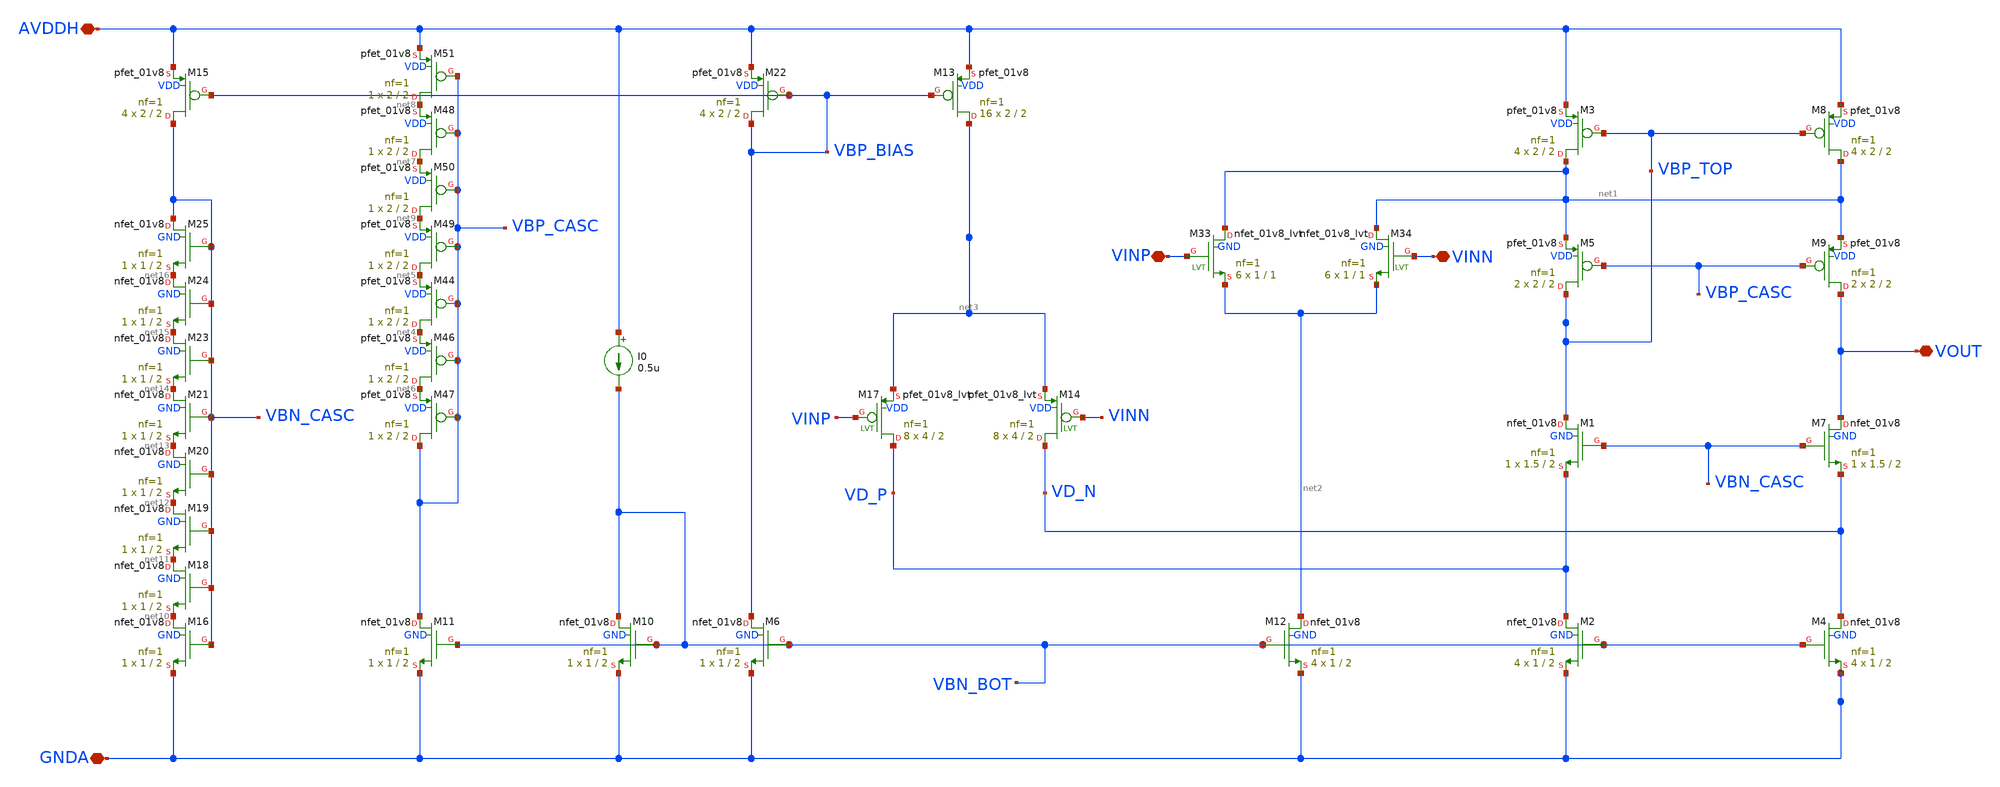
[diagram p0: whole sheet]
** sch_path: OTAs/N_OTA_with_internal_bias/OTA_Gm_Cell_v3.sch
**.subckt OTA_Gm_Cell_v3 AVDDH GNDA VOUT VINP VINN
*.iopin AVDDH
*.iopin GNDA
*.iopin VOUT
*.iopin VINP
*.iopin VINN
XM1 VBP_TOP VBN_CASC VD_P GND sky130_fd_pr__nfet_01v8 L=2 W=1.5 nf=1 ad='int((1 + 1)/2) * 1.5 / 1 * 0.29'
+ as='int((1 + 2)/2) * 1.5 / 1 * 0.29' pd='2*int((1 + 1)/2) * (1.5 / 1 + 0.29)' ps='2*int((1 + 2)/2) * (1.5 / 1 + 0.29)'
+ nrd='0.29 / 1.5 ' nrs='0.29 / 1.5 ' sa=0 sb=0 sd=0 mult=1 m=1
XM3 net1 VBP_TOP AVDDH VDD sky130_fd_pr__pfet_01v8 L=2 W=2 nf=1 ad='int((1 + 1)/2) * 2 / 1 * 0.29' as='int((1 + 2)/2) * 2 / 1 * 0.29'
+ pd='2*int((1 + 1)/2) * (2 / 1 + 0.29)' ps='2*int((1 + 2)/2) * (2 / 1 + 0.29)' nrd='0.29 / 2 ' nrs='0.29 / 2 '
+ sa=0 sb=0 sd=0 mult=4 m=4
XM5 VBP_TOP VBP_CASC net1 VDD sky130_fd_pr__pfet_01v8 L=2 W=2 nf=1 ad='int((1 + 1)/2) * 2 / 1 * 0.29'
+ as='int((1 + 2)/2) * 2 / 1 * 0.29' pd='2*int((1 + 1)/2) * (2 / 1 + 0.29)' ps='2*int((1 + 2)/2) * (2 / 1 + 0.29)'
+ nrd='0.29 / 2 ' nrs='0.29 / 2 ' sa=0 sb=0 sd=0 mult=2 m=2
XM7 VOUT VBN_CASC VD_N GND sky130_fd_pr__nfet_01v8 L=2 W=1.5 nf=1 ad='int((1 + 1)/2) * 1.5 / 1 * 0.29'
+ as='int((1 + 2)/2) * 1.5 / 1 * 0.29' pd='2*int((1 + 1)/2) * (1.5 / 1 + 0.29)' ps='2*int((1 + 2)/2) * (1.5 / 1 + 0.29)'
+ nrd='0.29 / 1.5 ' nrs='0.29 / 1.5 ' sa=0 sb=0 sd=0 mult=1 m=1
XM8 net1 VBP_TOP AVDDH VDD sky130_fd_pr__pfet_01v8 L=2 W=2 nf=1 ad='int((1 + 1)/2) * 2 / 1 * 0.29' as='int((1 + 2)/2) * 2 / 1 * 0.29'
+ pd='2*int((1 + 1)/2) * (2 / 1 + 0.29)' ps='2*int((1 + 2)/2) * (2 / 1 + 0.29)' nrd='0.29 / 2 ' nrs='0.29 / 2 '
+ sa=0 sb=0 sd=0 mult=4 m=4
XM9 VOUT VBP_CASC net1 VDD sky130_fd_pr__pfet_01v8 L=2 W=2 nf=1 ad='int((1 + 1)/2) * 2 / 1 * 0.29' as='int((1 + 2)/2) * 2 / 1 * 0.29'
+ pd='2*int((1 + 1)/2) * (2 / 1 + 0.29)' ps='2*int((1 + 2)/2) * (2 / 1 + 0.29)' nrd='0.29 / 2 ' nrs='0.29 / 2 '
+ sa=0 sb=0 sd=0 mult=2 m=2
XM33 net1 VINP net2 GND sky130_fd_pr__nfet_01v8_lvt L=1 W=1 nf=1 ad='int((1 + 1)/2) * 1 / 1 * 0.29' as='int((1 + 2)/2) * 1 / 1 * 0.29'
+ pd='2*int((1 + 1)/2) * (1 / 1 + 0.29)' ps='2*int((1 + 2)/2) * (1 / 1 + 0.29)' nrd='0.29 / 1 ' nrs='0.29 / 1 '
+ sa=0 sb=0 sd=0 mult=6 m=6
XM34 net1 VINN net2 GND sky130_fd_pr__nfet_01v8_lvt L=1 W=1 nf=1 ad='int((1 + 1)/2) * 1 / 1 * 0.29' as='int((1 + 2)/2) * 1 / 1 * 0.29'
+ pd='2*int((1 + 1)/2) * (1 / 1 + 0.29)' ps='2*int((1 + 2)/2) * (1 / 1 + 0.29)' nrd='0.29 / 1 ' nrs='0.29 / 1 '
+ sa=0 sb=0 sd=0 mult=6 m=6
XM44 net4 VBP_CASC net5 VDD sky130_fd_pr__pfet_01v8 L=2 W=2 nf=1 ad='int((1 + 1)/2) * 2 / 1 * 0.29' as='int((1 + 2)/2) * 2 / 1 * 0.29'
+ pd='2*int((1 + 1)/2) * (2 / 1 + 0.29)' ps='2*int((1 + 2)/2) * (2 / 1 + 0.29)' nrd='0.29 / 2 ' nrs='0.29 / 2 '
+ sa=0 sb=0 sd=0 mult=1 m=1
XM46 net6 VBP_CASC net4 VDD sky130_fd_pr__pfet_01v8 L=2 W=2 nf=1 ad='int((1 + 1)/2) * 2 / 1 * 0.29' as='int((1 + 2)/2) * 2 / 1 * 0.29'
+ pd='2*int((1 + 1)/2) * (2 / 1 + 0.29)' ps='2*int((1 + 2)/2) * (2 / 1 + 0.29)' nrd='0.29 / 2 ' nrs='0.29 / 2 '
+ sa=0 sb=0 sd=0 mult=1 m=1
XM47 VBP_CASC VBP_CASC net6 VDD sky130_fd_pr__pfet_01v8 L=2 W=2 nf=1 ad='int((1 + 1)/2) * 2 / 1 * 0.29'
+ as='int((1 + 2)/2) * 2 / 1 * 0.29' pd='2*int((1 + 1)/2) * (2 / 1 + 0.29)' ps='2*int((1 + 2)/2) * (2 / 1 + 0.29)'
+ nrd='0.29 / 2 ' nrs='0.29 / 2 ' sa=0 sb=0 sd=0 mult=1 m=1
XM48 net7 VBP_CASC net8 VDD sky130_fd_pr__pfet_01v8 L=2 W=2 nf=1 ad='int((1 + 1)/2) * 2 / 1 * 0.29' as='int((1 + 2)/2) * 2 / 1 * 0.29'
+ pd='2*int((1 + 1)/2) * (2 / 1 + 0.29)' ps='2*int((1 + 2)/2) * (2 / 1 + 0.29)' nrd='0.29 / 2 ' nrs='0.29 / 2 '
+ sa=0 sb=0 sd=0 mult=1 m=1
XM49 net5 VBP_CASC net9 VDD sky130_fd_pr__pfet_01v8 L=2 W=2 nf=1 ad='int((1 + 1)/2) * 2 / 1 * 0.29' as='int((1 + 2)/2) * 2 / 1 * 0.29'
+ pd='2*int((1 + 1)/2) * (2 / 1 + 0.29)' ps='2*int((1 + 2)/2) * (2 / 1 + 0.29)' nrd='0.29 / 2 ' nrs='0.29 / 2 '
+ sa=0 sb=0 sd=0 mult=1 m=1
XM50 net9 VBP_CASC net7 VDD sky130_fd_pr__pfet_01v8 L=2 W=2 nf=1 ad='int((1 + 1)/2) * 2 / 1 * 0.29' as='int((1 + 2)/2) * 2 / 1 * 0.29'
+ pd='2*int((1 + 1)/2) * (2 / 1 + 0.29)' ps='2*int((1 + 2)/2) * (2 / 1 + 0.29)' nrd='0.29 / 2 ' nrs='0.29 / 2 '
+ sa=0 sb=0 sd=0 mult=1 m=1
XM51 net8 VBP_CASC AVDDH VDD sky130_fd_pr__pfet_01v8 L=2 W=2 nf=1 ad='int((1 + 1)/2) * 2 / 1 * 0.29'
+ as='int((1 + 2)/2) * 2 / 1 * 0.29' pd='2*int((1 + 1)/2) * (2 / 1 + 0.29)' ps='2*int((1 + 2)/2) * (2 / 1 + 0.29)'
+ nrd='0.29 / 2 ' nrs='0.29 / 2 ' sa=0 sb=0 sd=0 mult=1 m=1
XM13 net3 VBP_BIAS AVDDH VDD sky130_fd_pr__pfet_01v8 L=2 W=2 nf=1 ad='int((1 + 1)/2) * 2 / 1 * 0.29'
+ as='int((1 + 2)/2) * 2 / 1 * 0.29' pd='2*int((1 + 1)/2) * (2 / 1 + 0.29)' ps='2*int((1 + 2)/2) * (2 / 1 + 0.29)'
+ nrd='0.29 / 2 ' nrs='0.29 / 2 ' sa=0 sb=0 sd=0 mult=16 m=16
XM14 VD_N VINN net3 VDD sky130_fd_pr__pfet_01v8_lvt L=2 W=4 nf=1 ad='int((1 + 1)/2) * 4 / 1 * 0.29' as='int((1 + 2)/2) * 4 / 1 * 0.29'
+ pd='2*int((1 + 1)/2) * (4 / 1 + 0.29)' ps='2*int((1 + 2)/2) * (4 / 1 + 0.29)' nrd='0.29 / 4 ' nrs='0.29 / 4 '
+ sa=0 sb=0 sd=0 mult=8 m=8
XM17 VD_P VINP net3 VDD sky130_fd_pr__pfet_01v8_lvt L=2 W=4 nf=1 ad='int((1 + 1)/2) * 4 / 1 * 0.29' as='int((1 + 2)/2) * 4 / 1 * 0.29'
+ pd='2*int((1 + 1)/2) * (4 / 1 + 0.29)' ps='2*int((1 + 2)/2) * (4 / 1 + 0.29)' nrd='0.29 / 4 ' nrs='0.29 / 4 '
+ sa=0 sb=0 sd=0 mult=8 m=8
XM22 VBP_BIAS VBP_BIAS AVDDH VDD sky130_fd_pr__pfet_01v8 L=2 W=2 nf=1 ad='int((1 + 1)/2) * 2 / 1 * 0.29'
+ as='int((1 + 2)/2) * 2 / 1 * 0.29' pd='2*int((1 + 1)/2) * (2 / 1 + 0.29)' ps='2*int((1 + 2)/2) * (2 / 1 + 0.29)'
+ nrd='0.29 / 2 ' nrs='0.29 / 2 ' sa=0 sb=0 sd=0 mult=4 m=4
XM2 VD_P VBN_BOT GNDA GND sky130_fd_pr__nfet_01v8 L=2 W=1 nf=1 ad='int((1 + 1)/2) * 1 / 1 * 0.29' as='int((1 + 2)/2) * 1 / 1 * 0.29'
+ pd='2*int((1 + 1)/2) * (1 / 1 + 0.29)' ps='2*int((1 + 2)/2) * (1 / 1 + 0.29)' nrd='0.29 / 1 ' nrs='0.29 / 1 '
+ sa=0 sb=0 sd=0 mult=4 m=4
XM4 VD_N VBN_BOT GNDA GND sky130_fd_pr__nfet_01v8 L=2 W=1 nf=1 ad='int((1 + 1)/2) * 1 / 1 * 0.29' as='int((1 + 2)/2) * 1 / 1 * 0.29'
+ pd='2*int((1 + 1)/2) * (1 / 1 + 0.29)' ps='2*int((1 + 2)/2) * (1 / 1 + 0.29)' nrd='0.29 / 1 ' nrs='0.29 / 1 '
+ sa=0 sb=0 sd=0 mult=4 m=4
XM6 VBP_BIAS VBN_BOT GNDA GND sky130_fd_pr__nfet_01v8 L=2 W=1 nf=1 ad='int((1 + 1)/2) * 1 / 1 * 0.29'
+ as='int((1 + 2)/2) * 1 / 1 * 0.29' pd='2*int((1 + 1)/2) * (1 / 1 + 0.29)' ps='2*int((1 + 2)/2) * (1 / 1 + 0.29)'
+ nrd='0.29 / 1 ' nrs='0.29 / 1 ' sa=0 sb=0 sd=0 mult=1 m=1
XM10 VBN_BOT VBN_BOT GNDA GND sky130_fd_pr__nfet_01v8 L=2 W=1 nf=1 ad='int((1 + 1)/2) * 1 / 1 * 0.29'
+ as='int((1 + 2)/2) * 1 / 1 * 0.29' pd='2*int((1 + 1)/2) * (1 / 1 + 0.29)' ps='2*int((1 + 2)/2) * (1 / 1 + 0.29)'
+ nrd='0.29 / 1 ' nrs='0.29 / 1 ' sa=0 sb=0 sd=0 mult=1 m=1
I0 AVDDH VBN_BOT 0.5u
XM11 VBP_CASC VBN_BOT GNDA GND sky130_fd_pr__nfet_01v8 L=2 W=1 nf=1 ad='int((1 + 1)/2) * 1 / 1 * 0.29'
+ as='int((1 + 2)/2) * 1 / 1 * 0.29' pd='2*int((1 + 1)/2) * (1 / 1 + 0.29)' ps='2*int((1 + 2)/2) * (1 / 1 + 0.29)'
+ nrd='0.29 / 1 ' nrs='0.29 / 1 ' sa=0 sb=0 sd=0 mult=1 m=1
XM12 net2 VBN_BOT GNDA GND sky130_fd_pr__nfet_01v8 L=2 W=1 nf=1 ad='int((1 + 1)/2) * 1 / 1 * 0.29' as='int((1 + 2)/2) * 1 / 1 * 0.29'
+ pd='2*int((1 + 1)/2) * (1 / 1 + 0.29)' ps='2*int((1 + 2)/2) * (1 / 1 + 0.29)' nrd='0.29 / 1 ' nrs='0.29 / 1 '
+ sa=0 sb=0 sd=0 mult=4 m=4
XM15 VBN_CASC VBP_BIAS AVDDH VDD sky130_fd_pr__pfet_01v8 L=2 W=2 nf=1 ad='int((1 + 1)/2) * 2 / 1 * 0.29'
+ as='int((1 + 2)/2) * 2 / 1 * 0.29' pd='2*int((1 + 1)/2) * (2 / 1 + 0.29)' ps='2*int((1 + 2)/2) * (2 / 1 + 0.29)'
+ nrd='0.29 / 2 ' nrs='0.29 / 2 ' sa=0 sb=0 sd=0 mult=4 m=4
XM16 net10 VBN_CASC GNDA GND sky130_fd_pr__nfet_01v8 L=2 W=1 nf=1 ad='int((1 + 1)/2) * 1 / 1 * 0.29'
+ as='int((1 + 2)/2) * 1 / 1 * 0.29' pd='2*int((1 + 1)/2) * (1 / 1 + 0.29)' ps='2*int((1 + 2)/2) * (1 / 1 + 0.29)'
+ nrd='0.29 / 1 ' nrs='0.29 / 1 ' sa=0 sb=0 sd=0 mult=1 m=1
XM18 net11 VBN_CASC net10 GND sky130_fd_pr__nfet_01v8 L=2 W=1 nf=1 ad='int((1 + 1)/2) * 1 / 1 * 0.29'
+ as='int((1 + 2)/2) * 1 / 1 * 0.29' pd='2*int((1 + 1)/2) * (1 / 1 + 0.29)' ps='2*int((1 + 2)/2) * (1 / 1 + 0.29)'
+ nrd='0.29 / 1 ' nrs='0.29 / 1 ' sa=0 sb=0 sd=0 mult=1 m=1
XM19 net12 VBN_CASC net11 GND sky130_fd_pr__nfet_01v8 L=2 W=1 nf=1 ad='int((1 + 1)/2) * 1 / 1 * 0.29'
+ as='int((1 + 2)/2) * 1 / 1 * 0.29' pd='2*int((1 + 1)/2) * (1 / 1 + 0.29)' ps='2*int((1 + 2)/2) * (1 / 1 + 0.29)'
+ nrd='0.29 / 1 ' nrs='0.29 / 1 ' sa=0 sb=0 sd=0 mult=1 m=1
XM20 net13 VBN_CASC net12 GND sky130_fd_pr__nfet_01v8 L=2 W=1 nf=1 ad='int((1 + 1)/2) * 1 / 1 * 0.29'
+ as='int((1 + 2)/2) * 1 / 1 * 0.29' pd='2*int((1 + 1)/2) * (1 / 1 + 0.29)' ps='2*int((1 + 2)/2) * (1 / 1 + 0.29)'
+ nrd='0.29 / 1 ' nrs='0.29 / 1 ' sa=0 sb=0 sd=0 mult=1 m=1
XM21 net14 VBN_CASC net13 GND sky130_fd_pr__nfet_01v8 L=2 W=1 nf=1 ad='int((1 + 1)/2) * 1 / 1 * 0.29'
+ as='int((1 + 2)/2) * 1 / 1 * 0.29' pd='2*int((1 + 1)/2) * (1 / 1 + 0.29)' ps='2*int((1 + 2)/2) * (1 / 1 + 0.29)'
+ nrd='0.29 / 1 ' nrs='0.29 / 1 ' sa=0 sb=0 sd=0 mult=1 m=1
XM23 net15 VBN_CASC net14 GND sky130_fd_pr__nfet_01v8 L=2 W=1 nf=1 ad='int((1 + 1)/2) * 1 / 1 * 0.29'
+ as='int((1 + 2)/2) * 1 / 1 * 0.29' pd='2*int((1 + 1)/2) * (1 / 1 + 0.29)' ps='2*int((1 + 2)/2) * (1 / 1 + 0.29)'
+ nrd='0.29 / 1 ' nrs='0.29 / 1 ' sa=0 sb=0 sd=0 mult=1 m=1
XM24 net16 VBN_CASC net15 GND sky130_fd_pr__nfet_01v8 L=2 W=1 nf=1 ad='int((1 + 1)/2) * 1 / 1 * 0.29'
+ as='int((1 + 2)/2) * 1 / 1 * 0.29' pd='2*int((1 + 1)/2) * (1 / 1 + 0.29)' ps='2*int((1 + 2)/2) * (1 / 1 + 0.29)'
+ nrd='0.29 / 1 ' nrs='0.29 / 1 ' sa=0 sb=0 sd=0 mult=1 m=1
XM25 VBN_CASC VBN_CASC net16 GND sky130_fd_pr__nfet_01v8 L=2 W=1 nf=1 ad='int((1 + 1)/2) * 1 / 1 * 0.29'
+ as='int((1 + 2)/2) * 1 / 1 * 0.29' pd='2*int((1 + 1)/2) * (1 / 1 + 0.29)' ps='2*int((1 + 2)/2) * (1 / 1 + 0.29)'
+ nrd='0.29 / 1 ' nrs='0.29 / 1 ' sa=0 sb=0 sd=0 mult=1 m=1
**.ends
.end
